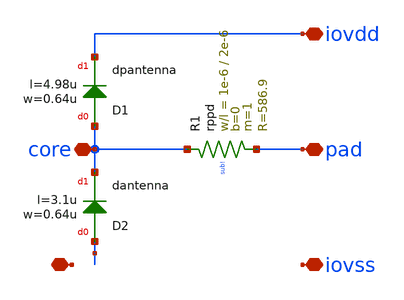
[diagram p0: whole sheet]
** sch_path: ihp-sg13g2/libs.tech/xschem/hm_stdcells/sg13g2_SecondaryProtection_noptap.sch
**.subckt sg13g2_SecondaryProtection_noptap iovss core pad iovdd !
*.iopin iovss
*.iopin core
*.iopin pad
*.iopin iovdd
*.iopin !
XD1 core iovdd dpantenna l=4.98u w=0.64u
XD2 ! core dantenna l=3.1u w=0.64u
XR1 core pad sub! rppd w=1e-6 l=2e-6 m=1 b=0 mm_ok=1
**.ends
.end
